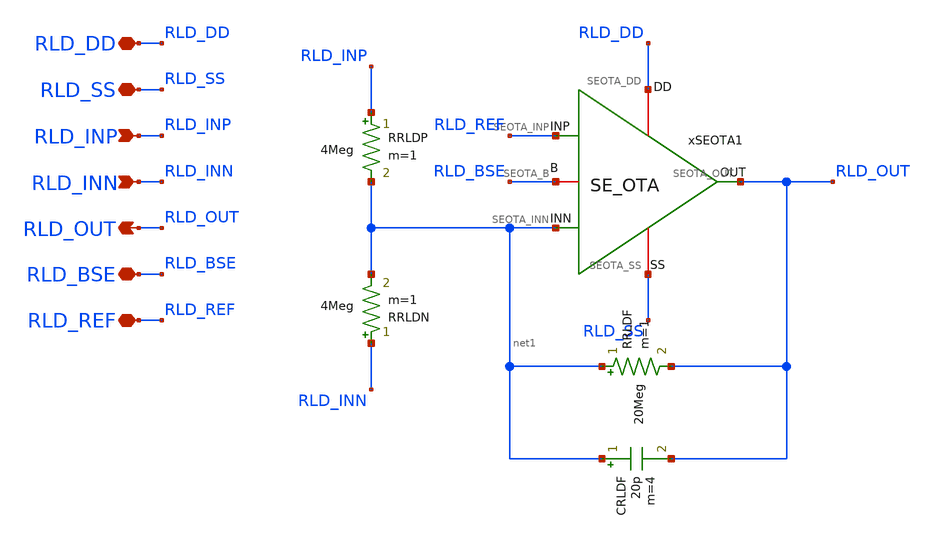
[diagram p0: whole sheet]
** sch_path: Design_Files/IC Design/Schematic/RLD/RLD.sch
**.subckt RLD RLD_DD RLD_SS RLD_INP RLD_INN RLD_OUT RLD_BSE RLD_REF
*.iopin RLD_DD
*.iopin RLD_SS
*.ipin RLD_INP
*.ipin RLD_INN
*.opin RLD_OUT
*.iopin RLD_BSE
*.iopin RLD_REF
xSEOTA1 RLD_DD RLD_SS RLD_REF net1 RLD_OUT RLD_BSE SE_OTA
RRLDP RLD_INP net1 4Meg m=1
RRLDN RLD_INN net1 4Meg m=1
RRLDF net1 RLD_OUT 20Meg m=1
CRLDF net1 RLD_OUT 20p m=4
**.ends

* expanding   symbol:  ECG_Acquisition_IC/Design_Files/IC Design/Schematic/SE_OTA/SE_OTA.sym # of
*+ pins=6
** sym_path: Design_Files/IC Design/Schematic/SE_OTA/SE_OTA.sym
** sch_path: Design_Files/IC Design/Schematic/SE_OTA/SE_OTA.sch
.subckt SE_OTA SEOTA_DD SEOTA_SS SEOTA_INP SEOTA_INN SEOTA_OUT SEOTA_B
*.iopin SEOTA_DD
*.iopin SEOTA_SS
*.ipin SEOTA_INP
*.ipin SEOTA_INN
*.opin SEOTA_OUT
*.iopin SEOTA_B
XM3 net4 net4 SEOTA_DD SEOTA_DD pfet_03v3 L=4u W=1u nf=1 ad='int((nf+1)/2) * W/nf * 0.18u' as='int((nf+2)/2) * W/nf * 0.18u'
+ pd='2*int((nf+1)/2) * (W/nf + 0.18u)' ps='2*int((nf+2)/2) * (W/nf + 0.18u)' nrd='0.18u / W' nrs='0.18u / W'
+ sa=0 sb=0 sd=0 m=60
XM7 SEOTA_OUT SEOTA_B SEOTA_SS SEOTA_SS nfet_03v3 L=0.5u W=1u nf=1 ad='int((nf+1)/2) * W/nf * 0.18u'
+ as='int((nf+2)/2) * W/nf * 0.18u' pd='2*int((nf+1)/2) * (W/nf + 0.18u)' ps='2*int((nf+2)/2) * (W/nf + 0.18u)'
+ nrd='0.18u / W' nrs='0.18u / W' sa=0 sb=0 sd=0 m=100
Rz net1 net2 3.8k m=1
XM5 net3 SEOTA_B SEOTA_SS SEOTA_SS nfet_03v3 L=2u W=1u nf=1 ad='int((nf+1)/2) * W/nf * 0.18u' as='int((nf+2)/2) * W/nf * 0.18u'
+ pd='2*int((nf+1)/2) * (W/nf + 0.18u)' ps='2*int((nf+2)/2) * (W/nf + 0.18u)' nrd='0.18u / W' nrs='0.18u / W'
+ sa=0 sb=0 sd=0 m=10
XM6 SEOTA_OUT net1 SEOTA_DD SEOTA_DD pfet_03v3 L=0.5u W=1u nf=1 ad='int((nf+1)/2) * W/nf * 0.18u' as='int((nf+2)/2) * W/nf * 0.18u'
+ pd='2*int((nf+1)/2) * (W/nf + 0.18u)' ps='2*int((nf+2)/2) * (W/nf + 0.18u)' nrd='0.18u / W' nrs='0.18u / W'
+ sa=0 sb=0 sd=0 m=400
XM8 SEOTA_B SEOTA_B SEOTA_SS SEOTA_SS nfet_03v3 L=2u W=1u nf=1 ad='int((nf+1)/2) * W/nf * 0.18u' as='int((nf+2)/2) * W/nf * 0.18u'
+ pd='2*int((nf+1)/2) * (W/nf + 0.18u)' ps='2*int((nf+2)/2) * (W/nf + 0.18u)' nrd='0.18u / W' nrs='0.18u / W'
+ sa=0 sb=0 sd=0 m=20
Cc net2 SEOTA_OUT 2p m=1
XM4 net1 net4 SEOTA_DD SEOTA_DD pfet_03v3 L=4u W=1u nf=1 ad='int((nf+1)/2) * W/nf * 0.18u' as='int((nf+2)/2) * W/nf * 0.18u'
+ pd='2*int((nf+1)/2) * (W/nf + 0.18u)' ps='2*int((nf+2)/2) * (W/nf + 0.18u)' nrd='0.18u / W' nrs='0.18u / W'
+ sa=0 sb=0 sd=0 m=60
XM1 net4 SEOTA_INN net3 SEOTA_SS nfet_03v3 L=4u W=1u nf=1 ad='int((nf+1)/2) * W/nf * 0.18u' as='int((nf+2)/2) * W/nf * 0.18u'
+ pd='2*int((nf+1)/2) * (W/nf + 0.18u)' ps='2*int((nf+2)/2) * (W/nf + 0.18u)' nrd='0.18u / W' nrs='0.18u / W'
+ sa=0 sb=0 sd=0 m=400
XM2 net1 SEOTA_INP net3 SEOTA_SS nfet_03v3 L=4u W=1u nf=1 ad='int((nf+1)/2) * W/nf * 0.18u' as='int((nf+2)/2) * W/nf * 0.18u'
+ pd='2*int((nf+1)/2) * (W/nf + 0.18u)' ps='2*int((nf+2)/2) * (W/nf + 0.18u)' nrd='0.18u / W' nrs='0.18u / W'
+ sa=0 sb=0 sd=0 m=400
.ends

.end
